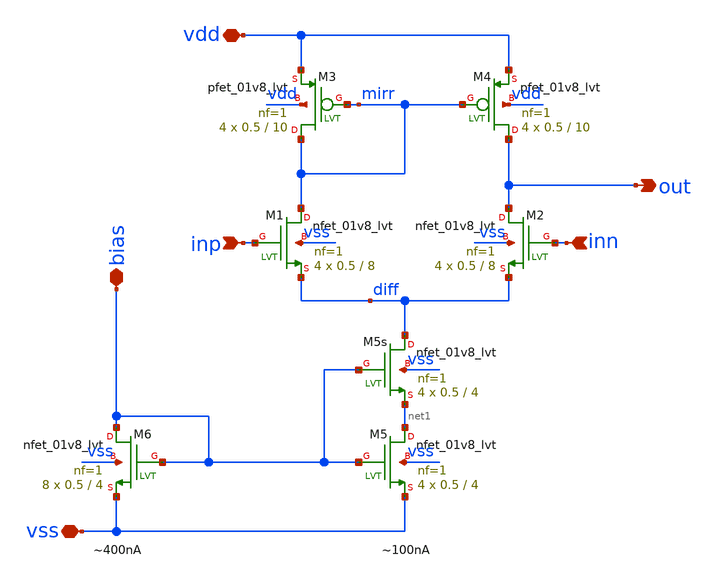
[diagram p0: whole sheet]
** sch_path: xschem/bias/bias_amp.sch
**.subckt bias_amp vdd bias inp inn out vss
*.iopin vdd
*.iopin bias
*.ipin inp
*.ipin inn
*.opin out
*.iopin vss
XM3 mirr mirr vdd vdd sky130_fd_pr__pfet_01v8_lvt L=10 W=0.5 nf=1 ad='int((nf+1)/2) * W/nf * 0.29' as='int((nf+2)/2) * W/nf * 0.29'
+ pd='2*int((nf+1)/2) * (W/nf + 0.29)' ps='2*int((nf+2)/2) * (W/nf + 0.29)' nrd='0.29 / W' nrs='0.29 / W'
+ sa=0 sb=0 sd=0 mult=4 m=4
XM4 out mirr vdd vdd sky130_fd_pr__pfet_01v8_lvt L=10 W=0.5 nf=1 ad='int((nf+1)/2) * W/nf * 0.29' as='int((nf+2)/2) * W/nf * 0.29'
+ pd='2*int((nf+1)/2) * (W/nf + 0.29)' ps='2*int((nf+2)/2) * (W/nf + 0.29)' nrd='0.29 / W' nrs='0.29 / W'
+ sa=0 sb=0 sd=0 mult=4 m=4
XM1 mirr inp diff vss sky130_fd_pr__nfet_01v8_lvt L=8 W=0.5 nf=1 ad='int((nf+1)/2) * W/nf * 0.29' as='int((nf+2)/2) * W/nf * 0.29'
+ pd='2*int((nf+1)/2) * (W/nf + 0.29)' ps='2*int((nf+2)/2) * (W/nf + 0.29)' nrd='0.29 / W' nrs='0.29 / W'
+ sa=0 sb=0 sd=0 mult=4 m=4
XM2 out inn diff vss sky130_fd_pr__nfet_01v8_lvt L=8 W=0.5 nf=1 ad='int((nf+1)/2) * W/nf * 0.29' as='int((nf+2)/2) * W/nf * 0.29'
+ pd='2*int((nf+1)/2) * (W/nf + 0.29)' ps='2*int((nf+2)/2) * (W/nf + 0.29)' nrd='0.29 / W' nrs='0.29 / W'
+ sa=0 sb=0 sd=0 mult=4 m=4
XM5 net1 bias vss vss sky130_fd_pr__nfet_01v8_lvt L=4 W=0.5 nf=1 ad='int((nf+1)/2) * W/nf * 0.29' as='int((nf+2)/2) * W/nf * 0.29'
+ pd='2*int((nf+1)/2) * (W/nf + 0.29)' ps='2*int((nf+2)/2) * (W/nf + 0.29)' nrd='0.29 / W' nrs='0.29 / W'
+ sa=0 sb=0 sd=0 mult=4 m=4
XM6 bias bias vss vss sky130_fd_pr__nfet_01v8_lvt L=4 W=0.5 nf=1 ad='int((nf+1)/2) * W/nf * 0.29' as='int((nf+2)/2) * W/nf * 0.29'
+ pd='2*int((nf+1)/2) * (W/nf + 0.29)' ps='2*int((nf+2)/2) * (W/nf + 0.29)' nrd='0.29 / W' nrs='0.29 / W'
+ sa=0 sb=0 sd=0 mult=8 m=8
XM5s diff bias net1 vss sky130_fd_pr__nfet_01v8_lvt L=4 W=0.5 nf=1 ad='int((nf+1)/2) * W/nf * 0.29' as='int((nf+2)/2) * W/nf * 0.29'
+ pd='2*int((nf+1)/2) * (W/nf + 0.29)' ps='2*int((nf+2)/2) * (W/nf + 0.29)' nrd='0.29 / W' nrs='0.29 / W'
+ sa=0 sb=0 sd=0 mult=4 m=4
**.ends
.end
